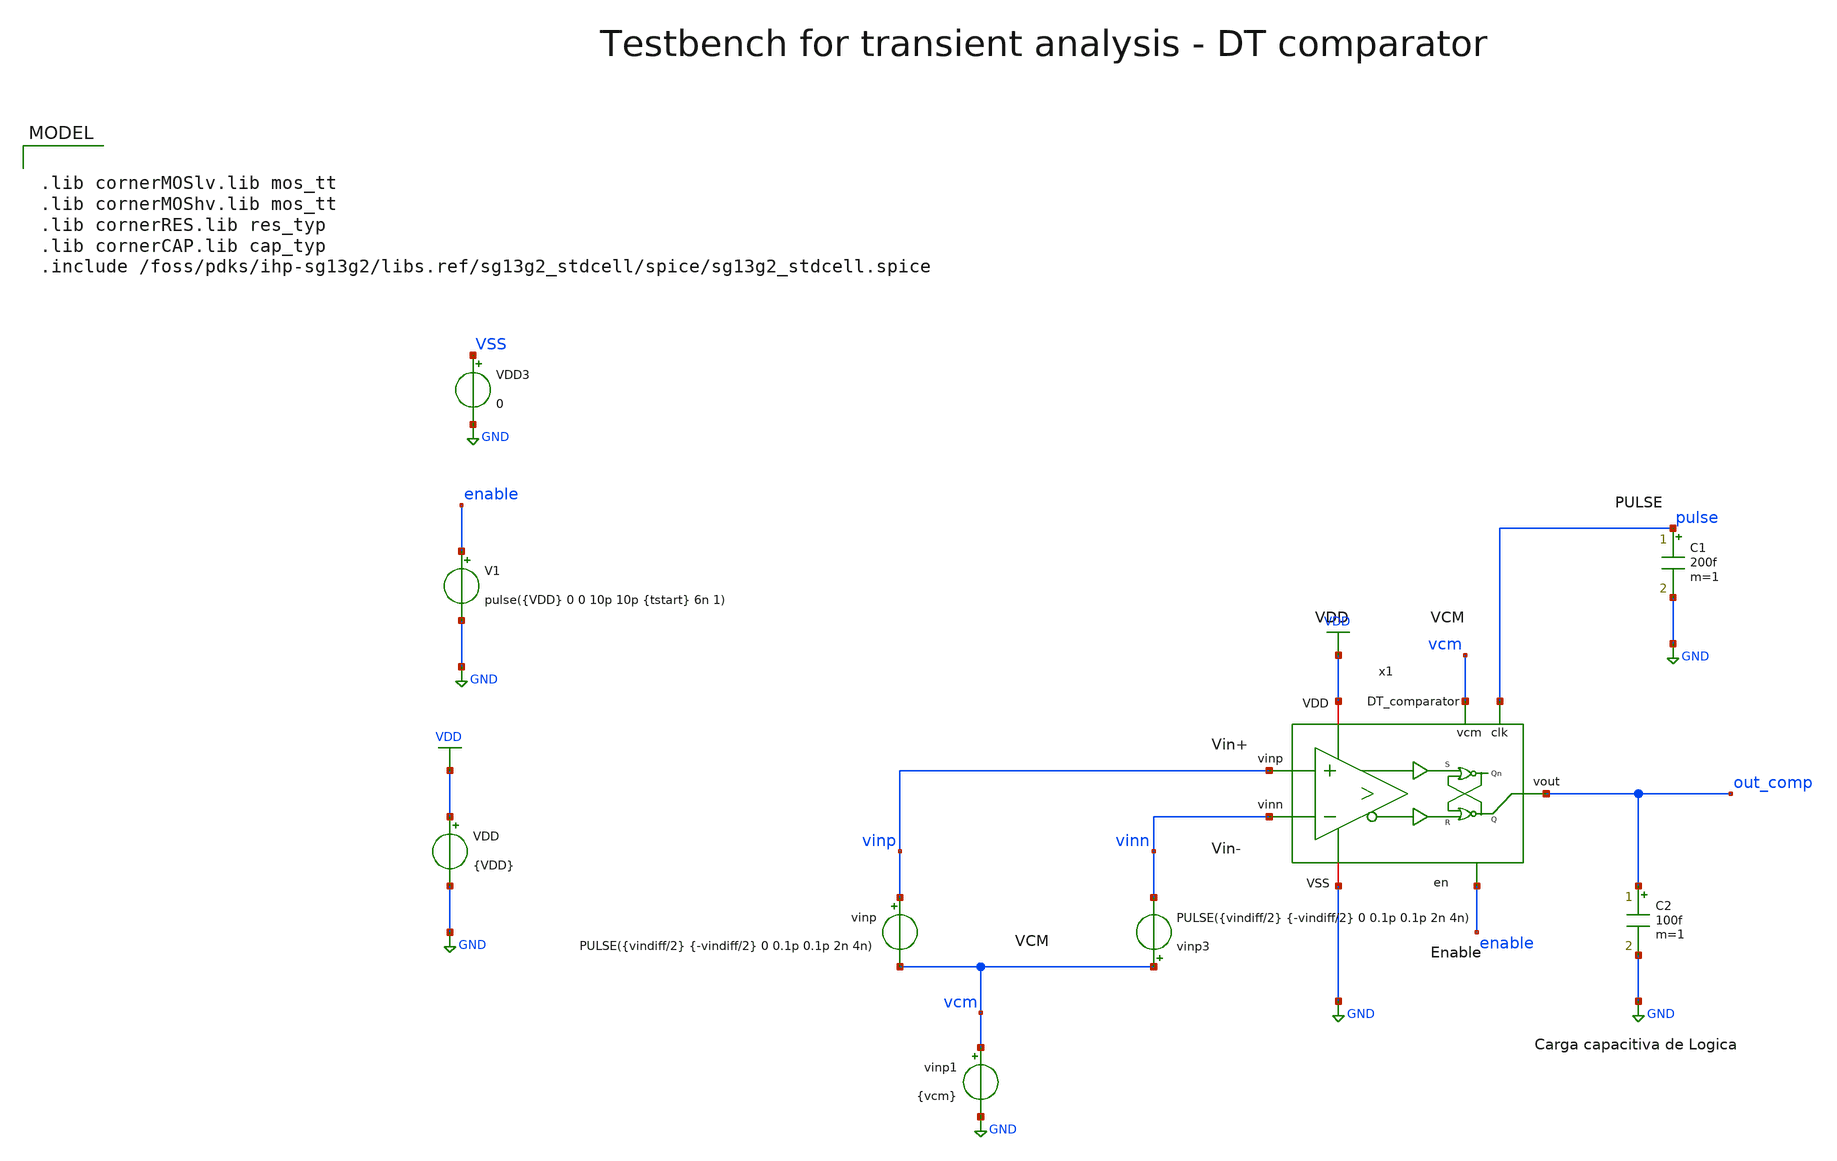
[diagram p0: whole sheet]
** sch_path: xschem/comparator/discrete_time/testbenches/DT_comparator_tb_tran.sch
**.subckt DT_comparator_tb_tran
VDD VDD GND {VDD}
V1 enable GND pulse({VDD} 0 0 10p 10p {tstart} 6n 1)
vinp vinp vcm PULSE({vindiff/2} {-vindiff/2} 0 0.1p 0.1p 2n 4n)
C2 out_comp GND 100f m=1
x1 VDD vinp out_comp vinn enable GND pulse vcm DT_comparator
VDD3 VSS GND 0
vinp1 vcm GND {vcm}
C1 pulse GND 200f m=1
vinp3 vcm vinn PULSE({vindiff/2} {-vindiff/2} 0 0.1p 0.1p 2n 4n)
**** begin user architecture code

.lib cornerMOSlv.lib mos_tt
.lib cornerMOShv.lib mos_tt
.lib cornerRES.lib res_typ
.lib cornerCAP.lib cap_typ
.include /foss/pdks/ihp-sg13g2/libs.ref/sg13g2_stdcell/spice/sg13g2_stdcell.spice



.param vdd=1.8
.param temp=27
.param tstart=2n
.param vindiff = 219m
.param Vcm=0.9

.options savecurrents reltol=1e-3 abstol=1e-12 gmin=1e-15
.ic v(vout) = 0
.control
save all
set hcopydevtype = svg
set color0 = white
set color1 = black

* Operating Point Analysis
op
remzerovec
write DT_comparator_tb_tran.raw
set appendwrite

* Transient Analysis
* tran 4p 20n
tran 1p 10n
write DT_comparator_tb_tran.raw v(vinp) v(vinn) v(vout)

* Measure vcpp_min & vcpn_min
*let tmeas = 1/fclk
*meas tran vcpp_min FIND qv(x1.x1.vcpp) at=tmeas
*meas tran vcpn_min FIND v(x1.x1.vcpn) at=tmeas

* Measure Propagation Delay
* Time from clock rising edge to 90% VDD of vout

meas tran t_dec1 TRIG v(x1.voutp_buf) VAL=1.62 RISE=1 TARG v(pulse) VAL=0.18 FALL=1
meas tran t_dec2 TRIG v(x1.voutp_buf) VAL=1.62 RISE=2 TARG v(pulse) VAL=0.18 FALL=2
meas tran t_dec3 TRIG v(x1.voutp_buf) VAL=1.62 RISE=3 TARG v(pulse) VAL=0.18 FALL=3

meas tran t_resetp TRIG pulse VAL=1.62 RISE=2 TARG pulse VAL=0.18 FALL=1
meas tran t_resetn TRIG pulse VAL=1.62 RISE=3 TARG pulse VAL=0.18 FALL=3


echo Primer tiempo de decision $&t_dec1 s
echo Segundo tiempo de decison $&t_dec3 s


echo Tiempo de espera $&t_reset3 s

* Calculate Energy / Conversion
* i_int in As
* energy_conv in Ws = J
let t_conv = tstart + t_dec
meas tran i_int INTEG i(VDD) from=tstart to=t_conv
let energy_conv = 1.5 * i_int

*let energy_conv_femto = energy_conv * 1e15
*echo Energy / Conversion $&energy_conv_femto fJ/conv

* Plotting

let vin_dif_mV = (vinp-vinn)*1000
let outp_Bindra = x1.voutp_comp
let outn_Bindra = x1.voutn_comp
let outp_Buffer = x1.voutp_buf
let outn_Buffer = x1.voutn_buf
let READY = x1.x6.READY
let Schmitt_in = x1.x6.vx
let Schmitt_out = x1.x6.vxs
let Schmitt_outn = x1.x6.vx_n

plot i(VDD)
plot v(x1.voutp_buf) {v(x1.voutn_buf)} {v(x1.x6.vx_n) + 4}  {v(pulse) + 8} {v(x1.x6.READY) + 10}
plot v(x1.voutp_comp) {v(x1.voutn_comp)} {v(x1.x6.vx_n) + 4}  {v(x1.x6.vx) + 8} {v(x1.x6.vxs) + 10} vin_dif_mV+12
plot x1.voutp_comp pulse x1.voutp_buf x1.x6.ready
plot x1.voutp_comp x1.voutn_comp x1.x1.vcpp+2 x1.x1.vcpn+2 x1.x1.vs+4 x1.x1.vcap+4 pulse+6

hardcopy ./../../img/corriente_comparador.svg i(VDD) title 'consumo'
hardcopy ./../../img/salidas_internas_comparador.svg outp_Bindra outn_Bindra outp_Buffer+2 outn_Buffer+2
+ pulse+4 vin_dif_mV+6 title 'Salidas Internas del Comparador'
hardcopy ./../../img/senales_pgen.svg READY Schmitt_out+2 Schmitt_outn+2 Schmitt_in+2 pulse+4 title 'Señales Internas Generador de Pulsos'
hardcopy ./../../img/retardo_buffer_comp.svg outp_Bindra outn_Bindra+2 outp_Buffer outn_Buffer+2 out_comp+4
+ title 'Retardo Salidas'
hardcopy ./../../img/salidas_comp.svg vin_dif_mV out_comp pulse+4 enable+2 title 'Salidas Comparador'
hardcopy ./../../img/tiempo_rst_comp.svg pulse+2 outp_Bindra outn_Bindra xlimit 2.65n 2.95n title 'Tiempo Reset'



* Writing Data
set wr_singlescale
set wr_vecnames
let vs=x1.x1.vs
let vcpp=x1.x1.vcpp
let vcpn=x1.x1.vcpn
let voutp_comp=x1.voutp_comp
let voutn_comp=x1.voutn_comp
wrdata ./../../DT_comparator_tb_tran.txt v(clk) v(vinp) v(vinn) v(vs) v(vcpp) v(vcpn) v(voutp_comp)
+ v(voutn_comp) v(vout)

*quit
.endc

**** end user architecture code
**.ends
.GLOBAL GND
.GLOBAL VDD
.end
